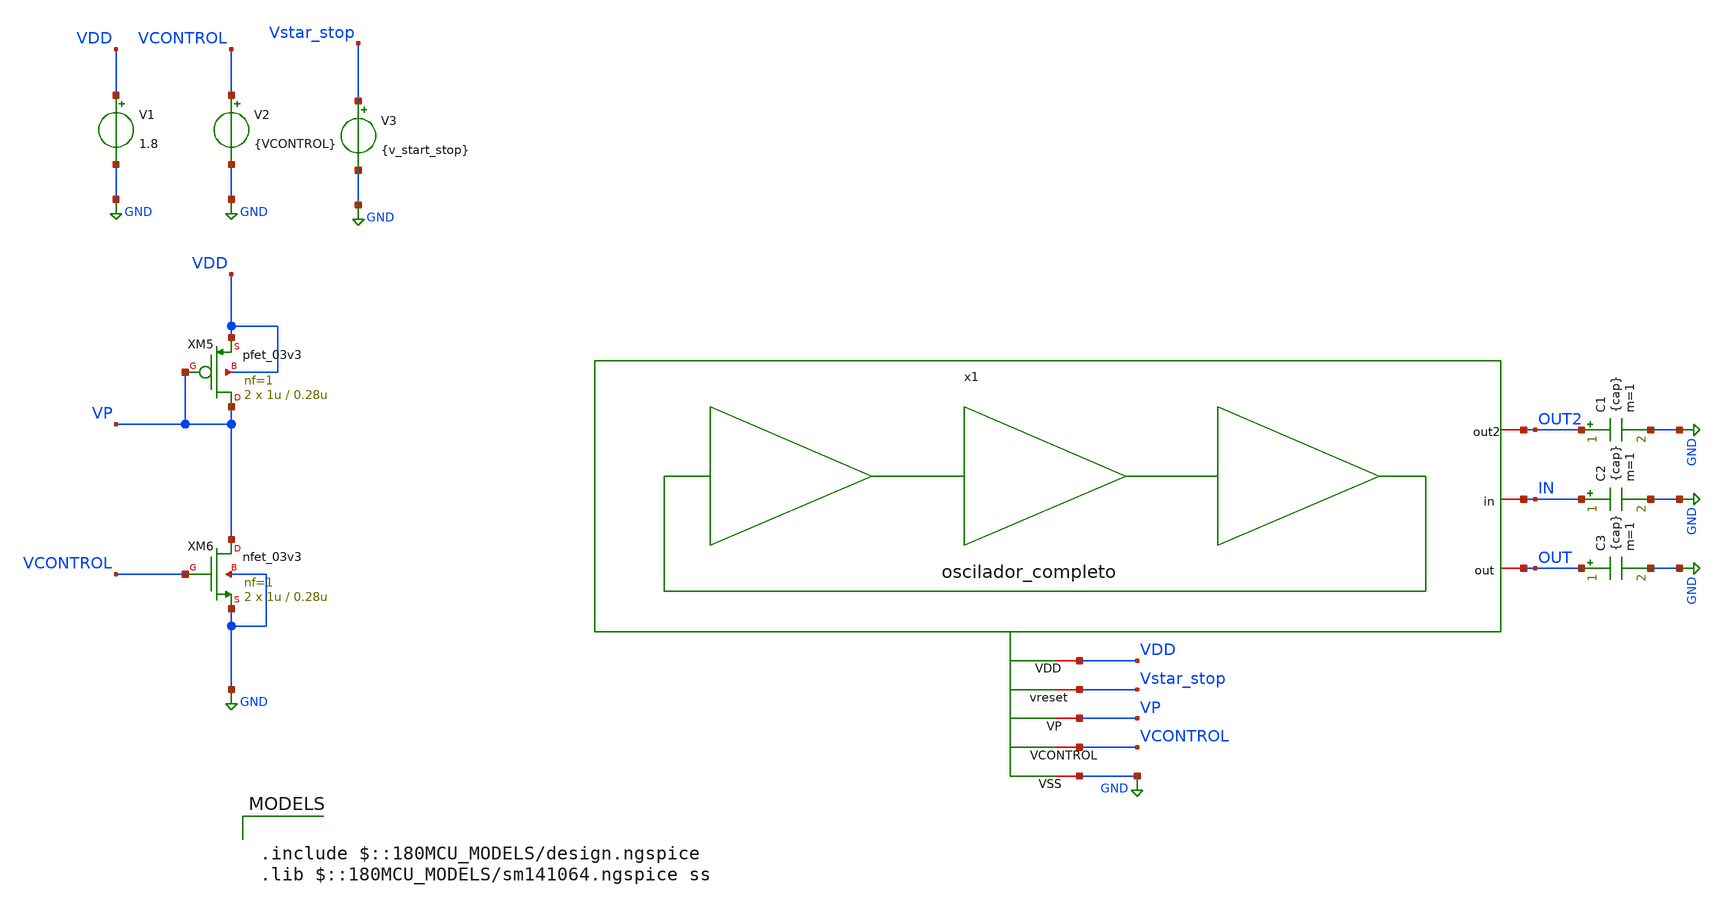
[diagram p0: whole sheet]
** sch_path: designs/ring_oscillator_pg/oscilador_prueba.sch
**.subckt oscilador_prueba
XM5 VP VP VDD VDD pfet_03v3 L=0.28u W=1u nf=1 ad='int((nf+1)/2) * W/nf * 0.18u' as='int((nf+2)/2) * W/nf * 0.18u'
+ pd='2*int((nf+1)/2) * (W/nf + 0.18u)' ps='2*int((nf+2)/2) * (W/nf + 0.18u)' nrd='0.18u / W' nrs='0.18u / W'
+ sa=0 sb=0 sd=0 m=2
XM6 VP VCONTROL GND GND nfet_03v3 L=0.28u W=1u nf=1 ad='int((nf+1)/2) * W/nf * 0.18u' as='int((nf+2)/2) * W/nf * 0.18u'
+ pd='2*int((nf+1)/2) * (W/nf + 0.18u)' ps='2*int((nf+2)/2) * (W/nf + 0.18u)' nrd='0.18u / W' nrs='0.18u / W'
+ sa=0 sb=0 sd=0 m=2
V1 VDD GND 1.8
V2 VCONTROL GND {VCONTROL}
V3 Vstar_stop GND {v_start_stop}
C1 OUT2 GND {cap} m=1
C2 IN GND {cap} m=1
C3 OUT GND {cap} m=1
x1 OUT2 IN OUT VDD Vstar_stop VP VCONTROL GND oscilador_completo
**** begin user architecture code

.include $::180MCU_MODELS/design.ngspice
.lib $::180MCU_MODELS/sm141064.ngspice ss




.TRAN 0.01n 1u
.param vcontrol=1
.param w=1u
.param wp=3.5u
.param cap=15f
.save v(out)
.param v_start_stop=0
.control

*----------------------------- Parámetros generales
let VP = 1.8
let per50 = VP * 0.5

*----------------------------- Parámetros para barrido de vcontrol (w = 100u)
let vstart = 0
let vend   = vp
let vstep  = 0.083
let npoints = (vend - vstart)/vstep+1
let vpp = vector(npoints)
let v = vstart
let idx = 0

*----------------------------- Crear vectores para vcontrol
let vcontrol_vec = vector(npoints)
let freq_vec     = vector(npoints)
settype voltage   vcontrol_vec
settype frequency freq_vec
alterparam w = 1u

*----------------------------- Parámetros para barrido de w (vcontrol = 0.8)
let wstart = 0.22u
let wend   = 10u
let wstep  = 0.035u
let wpoints = (wend - wstart)/wstep + 1
let w = wstart
let j = 0

*----------------------------- Crear vectores para w
let w_vec     = vector(wpoints)
let freqw_vec = vector(wpoints)
settype dimension  w_vec
settype frequency  freqw_vec

*==========================================================
*--------------------- BARRIDO vcontrol -------------------
*==========================================================
while v le vend
  alterparam vcontrol = $&v
  reset
  tran 0.01n 1u
  meas TRAN T_period TRIG v(out) VAL=per50 rise=2 TARG v(out) VAL=per50 rise=3
  let F_recu = 1 / T_period
  let vcontrol_vec[idx] = v
  let freq_vec[idx]     = F_recu
  let vpp[idx]=$v(vp)
  let v = v + vstep
  let idx = idx + 1
end

*==========================================================
*--------------------- BARRIDO w --------------------------
*==========================================================
alterparam vcontrol = 0.8
*while w le wend
 *alterparam w = $&w
 * reset
  *tran 0.01n 0.1u
 * meas TRAN T_period TRIG v(out) VAL=per50 rise=2 TARG v(out) VAL=per50 rise=3
 * let F_recu = 1 / T_period
  *let w_vec[j]     = w
  *let freqw_vec[j] = F_recu
  *let w = w + wstep
 *let j = j + 1
end

*==========================================================
*---------------------- PLOTS -----------------------------
*==========================================================
plot freq_vec   vs vcontrol_vec
*plot freqw_vec  vs w_vec

print vcontrol_vec freq_vec vpp
*print w_vec freqw_vec

.endc




.control
.param vcontrol=0.8
.param w=1u
.param wp=3.5u
.param cap=15f
.param v_start_stop=0

save all
save @m.xm5.m0[id]
save @m.xm6.m0[id]

* Pulso con 50ns en bajo y 50ns en alto, repitiéndose cada 100ns
alter @v3[PULSE]=(0 1.8 0 1n 1n 0.25u 0.5u)
TRAN 0.01n 1u

let VP=1.8
let per10 = Vp*0.1
let per50 = Vp*0.5
let per90 = Vp*0.9

meas TRAN t_rise  TRIG v(out) VAL=per10 rise=2  TARG v(out) VAL=per90 rise=2
meas TRAN t_fall  TRIG v(out) VAL=per90 fall=2  TARG v(out) VAL=per10 fall=2
meas TRAN t_delay  TRIG v(in) VAL=per50 rise=1 TARG v(out) VAL=per50 fall=1
meas TRAN T_period TRIG v(out) VAL=per50 rise=2 TARG v(out) VAL=per50 rise=3
let F_recu=1/T_period

echo '==============TRAN measurements========='

print t_delay
print t_rise
print t_fall
print T_period
print F_recu
print T_period/2

plot v(out) v(in) v(out2)
plot v(vstar_stop)
write ocilador_segunda_prueba.raw
.endc


**** end user architecture code
**.ends

* expanding   symbol:  gf180/ring_oscillator_pg/oscilador_completo.sym # of pins=8
** sym_path: designs/ring_oscillator_pg/oscilador_completo.sym
** sch_path: designs/ring_oscillator_pg/oscilador_completo.sch
.subckt oscilador_completo out2 in out VDD vreset VP VCONTROL VSS
*.iopin in
*.iopin out
*.iopin out2
*.iopin VDD
*.iopin VP
*.iopin VCONTROL
*.iopin VSS
*.iopin vreset
XM2 in vreset VSS VSS nfet_03v3 L=0.28u W=1u nf=1 ad='int((nf+1)/2) * W/nf * 0.18u' as='int((nf+2)/2) * W/nf * 0.18u'
+ pd='2*int((nf+1)/2) * (W/nf + 0.18u)' ps='2*int((nf+2)/2) * (W/nf + 0.18u)' nrd='0.18u / W' nrs='0.18u / W'
+ sa=0 sb=0 sd=0 m=2
x1 VDD VP in out2 VCONTROL VSS inversor
x2 VDD VP out in VCONTROL VSS inversor
x3 VDD VP out2 out VCONTROL VSS inversor
.ends


* expanding   symbol:  gf180/ring_oscillator_pg/inversor.sym # of pins=6
** sym_path: designs/ring_oscillator_pg/inversor.sym
** sch_path: designs/ring_oscillator_pg/inversor.sch
.subckt inversor VDD VP B A VCONTROL VSS
*.iopin B
*.iopin A
*.iopin VCONTROL
*.iopin VDD
*.iopin VP
*.iopin VSS
XM1 B A net1 VSS nfet_03v3 L=0.3u W={w} nf=1 ad='int((nf+1)/2) * W/nf * 0.18u' as='int((nf+2)/2) * W/nf * 0.18u'
+ pd='2*int((nf+1)/2) * (W/nf + 0.18u)' ps='2*int((nf+2)/2) * (W/nf + 0.18u)' nrd='0.18u / W' nrs='0.18u / W'
+ sa=0 sb=0 sd=0 m=1
XM2 B A net2 VDD pfet_03v3 L=0.3u W={wp} nf=1 ad='int((nf+1)/2) * W/nf * 0.18u' as='int((nf+2)/2) * W/nf * 0.18u'
+ pd='2*int((nf+1)/2) * (W/nf + 0.18u)' ps='2*int((nf+2)/2) * (W/nf + 0.18u)' nrd='0.18u / W' nrs='0.18u / W'
+ sa=0 sb=0 sd=0 m=1
XM3 net1 VCONTROL VSS VSS nfet_03v3 L=0.3u W={w} nf=1 ad='int((nf+1)/2) * W/nf * 0.18u' as='int((nf+2)/2) * W/nf * 0.18u'
+ pd='2*int((nf+1)/2) * (W/nf + 0.18u)' ps='2*int((nf+2)/2) * (W/nf + 0.18u)' nrd='0.18u / W' nrs='0.18u / W'
+ sa=0 sb=0 sd=0 m=2
XM4 net2 VP VDD VDD pfet_03v3 L=0.3u W={wp} nf=1 ad='int((nf+1)/2) * W/nf * 0.18u' as='int((nf+2)/2) * W/nf * 0.18u'
+ pd='2*int((nf+1)/2) * (W/nf + 0.18u)' ps='2*int((nf+2)/2) * (W/nf + 0.18u)' nrd='0.18u / W' nrs='0.18u / W'
+ sa=0 sb=0 sd=0 m=1
.ends

.GLOBAL GND
.end
